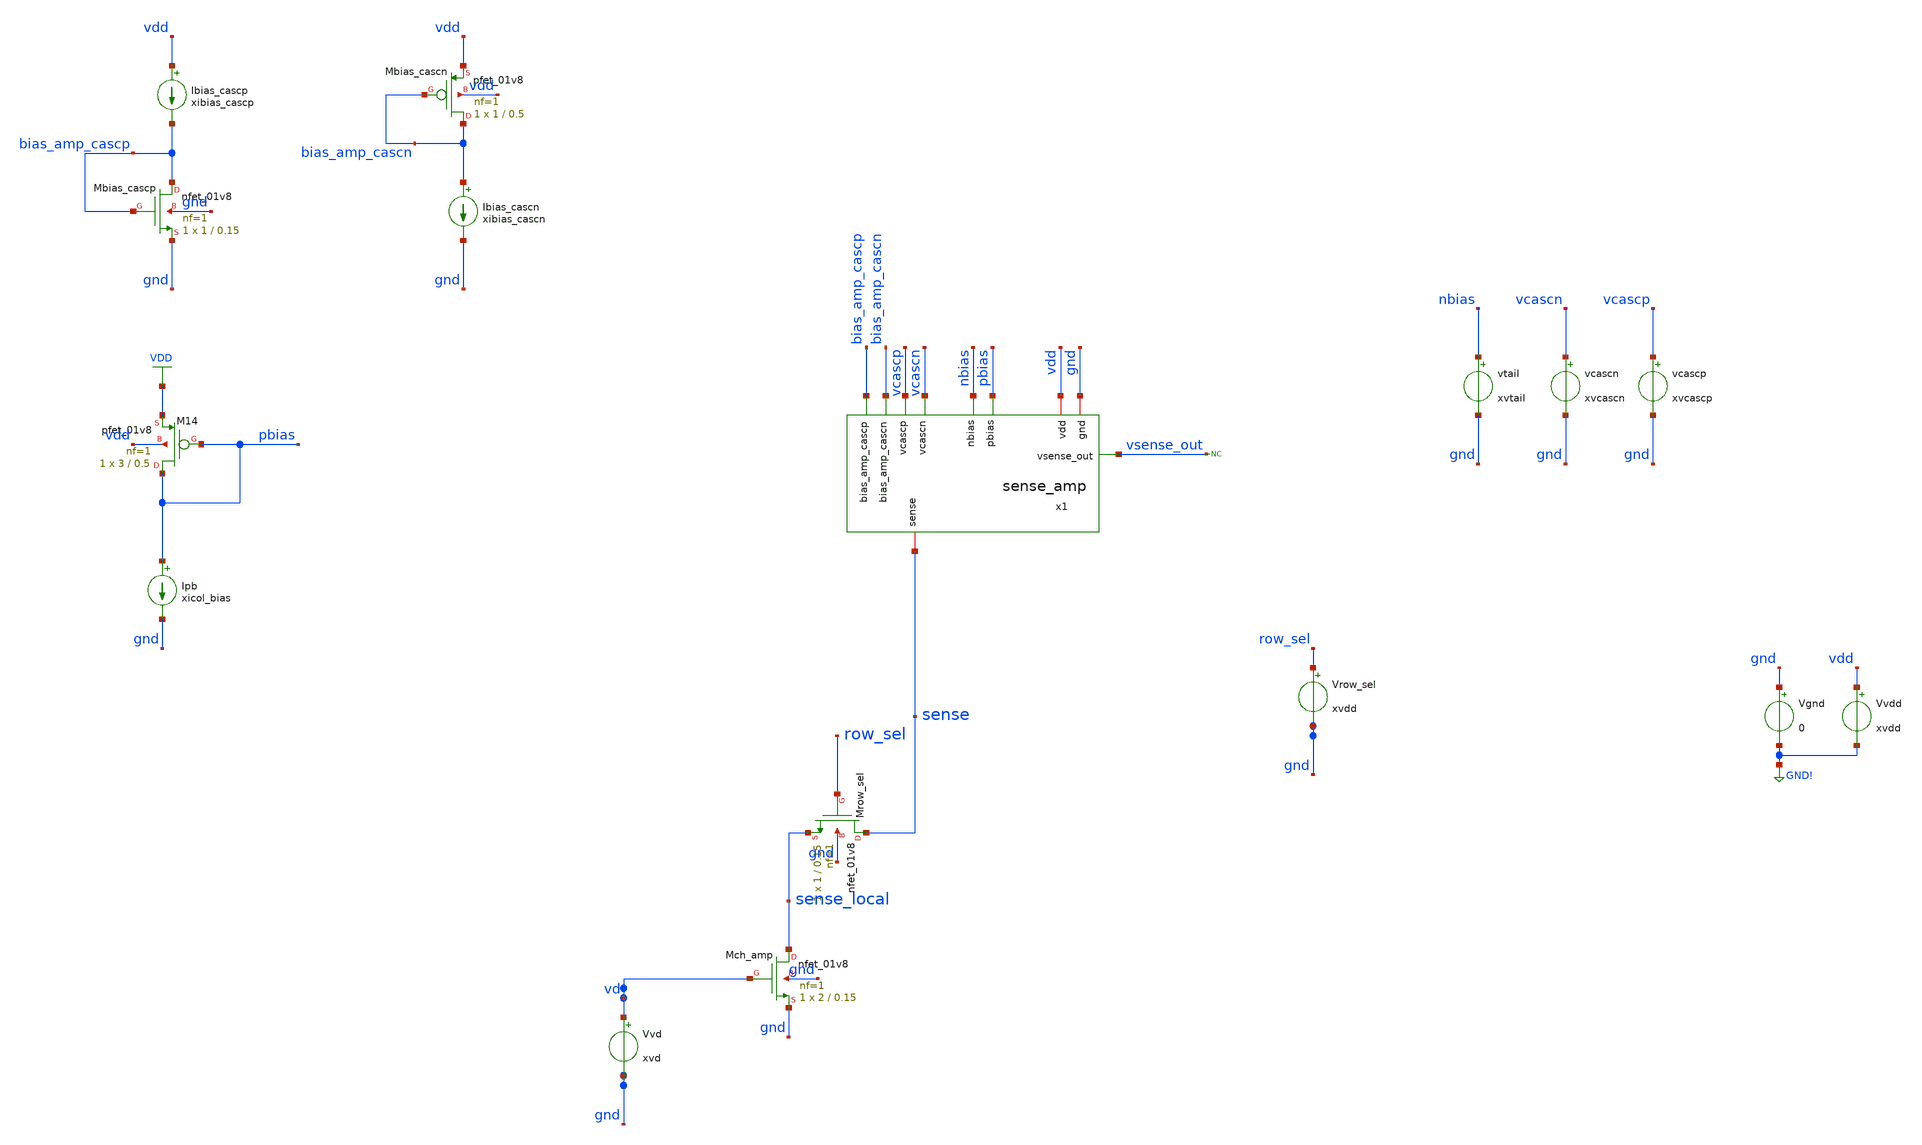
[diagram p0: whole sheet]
** sch_path: analog/klayout/production/final_merge_20260923/testbenches/cace/analog/xschem/test_sense_amp.sch
**.subckt test_sense_amp
XMch_amp sense_local vd gnd gnd sky130_fd_pr__nfet_01v8 L=0.15 W=2 nf=1 ad='int((1 + 1)/2) * 2 / 1 * 0.29'
+ as='int((1 + 2)/2) * 2 / 1 * 0.29' pd='2*int((1 + 1)/2) * (2 / 1 + 0.29)' ps='2*int((1 + 2)/2) * (2 / 1 + 0.29)'
+ nrd='0.29 / 2 ' nrs='0.29 / 2 ' sa=0 sb=0 sd=0 mult=1 m=1
XMrow_sel sense row_sel sense_local gnd sky130_fd_pr__nfet_01v8 L=0.15 W=1 nf=1 ad='int((1 + 1)/2) * 1 / 1 * 0.29'
+ as='int((1 + 2)/2) * 1 / 1 * 0.29' pd='2*int((1 + 1)/2) * (1 / 1 + 0.29)' ps='2*int((1 + 2)/2) * (1 / 1 + 0.29)'
+ nrd='0.29 / 1 ' nrs='0.29 / 1 ' sa=0 sb=0 sd=0 mult=1 m=1
vtail nbias gnd xvtail
vcascn vcascn gnd xvcascn
vcascp vcascp gnd xvcascp
Vgnd gnd GND! 0
Vvdd vdd GND! xvdd
Ipb pbias gnd xicol_bias
XM14 pbias pbias VDD vdd sky130_fd_pr__pfet_01v8 L=0.5 W=3 nf=1 ad='int((1 + 1)/2) * 3 / 1 * 0.29' as='int((1 + 2)/2) * 3 / 1 * 0.29'
+ pd='2*int((1 + 1)/2) * (3 / 1 + 0.29)' ps='2*int((1 + 2)/2) * (3 / 1 + 0.29)' nrd='0.29 / 3 ' nrs='0.29 / 3 '
+ sa=0 sb=0 sd=0 mult=1 m=1
XMbias_cascp bias_amp_cascp bias_amp_cascp gnd gnd sky130_fd_pr__nfet_01v8 L=0.15 W=1 nf=1 ad='int((1 + 1)/2) * 1 / 1 * 0.29'
+ as='int((1 + 2)/2) * 1 / 1 * 0.29' pd='2*int((1 + 1)/2) * (1 / 1 + 0.29)' ps='2*int((1 + 2)/2) * (1 / 1 + 0.29)'
+ nrd='0.29 / 1 ' nrs='0.29 / 1 ' sa=0 sb=0 sd=0 mult=1 m=1
Ibias_cascp vdd bias_amp_cascp xibias_cascp
XMbias_cascn bias_amp_cascn bias_amp_cascn vdd vdd sky130_fd_pr__pfet_01v8 L=0.5 W=1 nf=1 ad='int((1 + 1)/2) * 1 / 1 * 0.29'
+ as='int((1 + 2)/2) * 1 / 1 * 0.29' pd='2*int((1 + 1)/2) * (1 / 1 + 0.29)' ps='2*int((1 + 2)/2) * (1 / 1 + 0.29)'
+ nrd='0.29 / 1 ' nrs='0.29 / 1 ' sa=0 sb=0 sd=0 mult=1 m=1
Ibias_cascn bias_amp_cascn gnd xibias_cascn
Vrow_sel row_sel gnd xvdd
Vvd vd gnd xvd
x1 vdd pbias vcascp bias_amp_cascn vsense_out vcascn bias_amp_cascp gnd sense nbias sense_amp
* noconn vsense_out
**** begin user architecture code

* sim
*.option reltol=1e-3 abstol=1e-12 vntol=1e-5 gmin=1e-10
*.option trtol=6 chgtol=1e-12

.param xvcascn = 0.2
.param xvcascp = 1.6
.param xicol_bias = 5e-7
.param xvtail = 0.5
.param xvdd = 1.8
.param xvd = 0.1
.param xibias_cascp = 50n
.param xibias_cascn = 50n
.param xibias_comp = 50n

.control
save all
dc Vvd 0 1.8 10m
*op
write test_sense_amp_dc.raw
.endc



** opencircuitdesign pdks install
.lib $::SKYWATER_MODELS/sky130.lib.spice tt

**** end user architecture code
**.ends
.GLOBAL GND!
.GLOBAL VDD
.end
